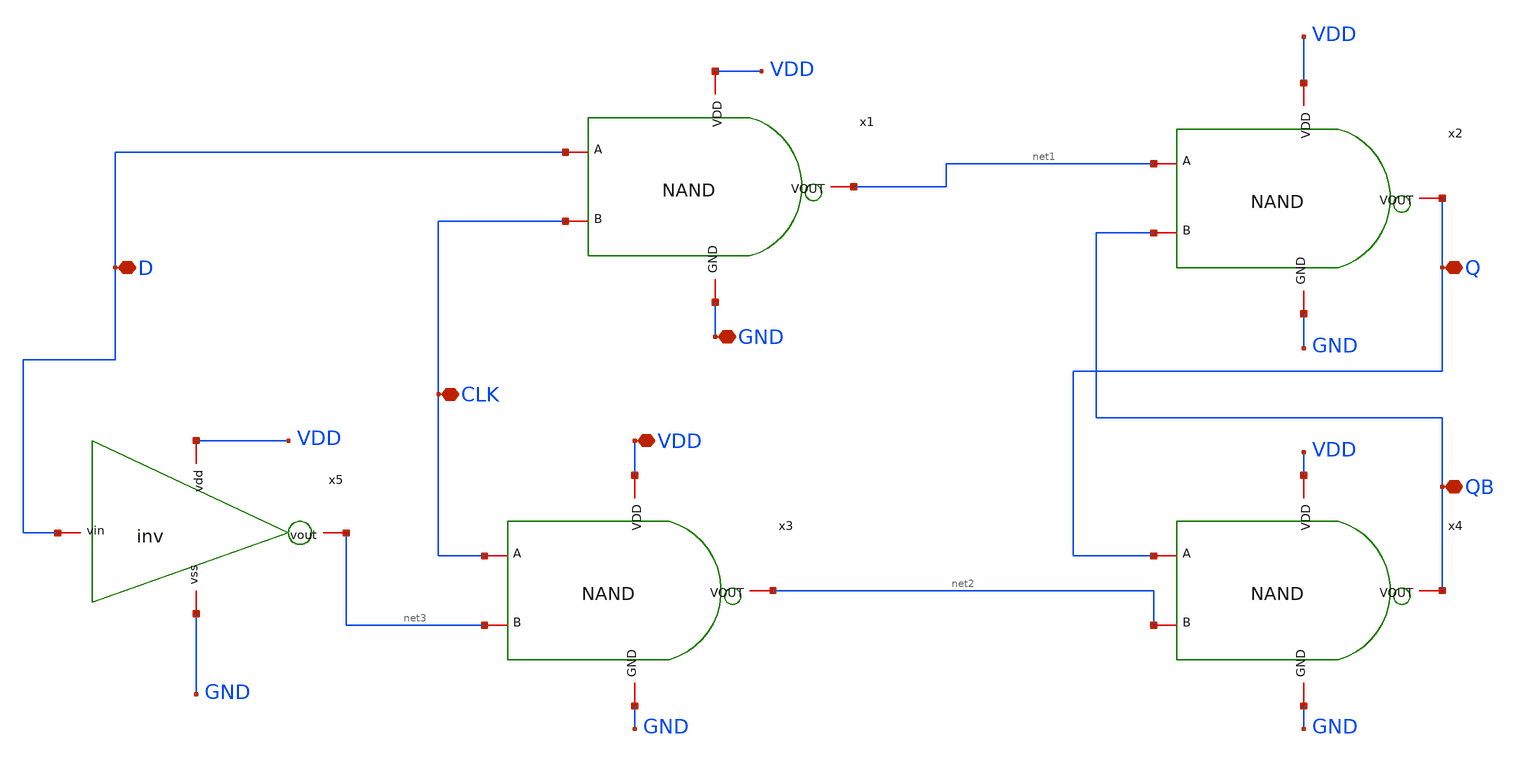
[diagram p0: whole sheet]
** sch_path: src/pixel/SRlatch.sch
**.subckt SRlatch D CLK VDD GND Q QB
*.iopin D
*.iopin CLK
*.iopin VDD
*.iopin GND
*.iopin Q
*.iopin QB
x1 VDD net1 CLK D GND NAND
x2 VDD Q QB net1 GND NAND
x3 VDD net2 net3 CLK GND NAND
x4 VDD QB net2 Q GND NAND
x5 VDD D net3 GND inv
**.ends
.end
